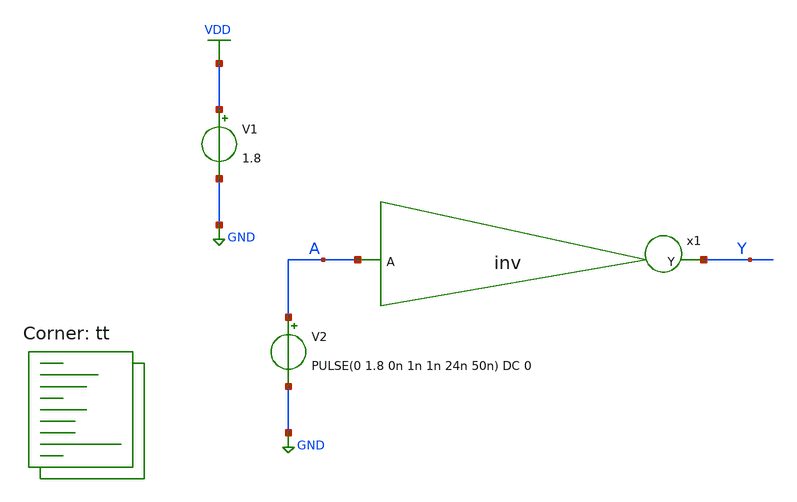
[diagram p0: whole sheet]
** sch_path: eng331lab_final/eng331lab_xschem/tb_inv2.sch
**.subckt tb_inv2
V1 VDD GND 1.8
V2 A GND PULSE(0 1.8 0n 1n 1n 24n 50n) DC 0
x1 Y A inv
**** begin user architecture code

.control
  save all
  tran 10n 400n
  write tb_inv2.raw
  set appendwirte
.endc


.lib $::SKYWATER_MODELS/sky130.lib.spice tt
**** end user architecture code
**.ends

* expanding   symbol:  eng331lab_xschem/inv.sym # of pins=2
** sym_path: eng331lab_final/eng331lab_xschem/inv.sym
** sch_path: eng331lab_final/eng331lab_xschem/inv.sch
.subckt inv Y A
*.ipin A
*.opin Y
XM1 Y A VDD VDD sky130_fd_pr__pfet_01v8 L=0.15 W=0.8 nf=1 ad='int((1 + 1)/2) * 0.8 / 1 * 0.29' as='int((1 + 2)/2) * 0.8 / 1 * 0.29'
+ pd='2*int((1 + 1)/2) * (0.8 / 1 + 0.29)' ps='2*int((1 + 2)/2) * (0.8 / 1 + 0.29)' nrd='0.29 / 0.8 ' nrs='0.29 / 0.8 '
+ sa=0 sb=0 sd=0 mult=1 m=1
XM2 Y A GND GND sky130_fd_pr__nfet_01v8 L=0.15 W=0.5 nf=1 ad='int((1 + 1)/2) * 0.5 / 1 * 0.29' as='int((1 + 2)/2) * 0.5 / 1 * 0.29'
+ pd='2*int((1 + 1)/2) * (0.5 / 1 + 0.29)' ps='2*int((1 + 2)/2) * (0.5 / 1 + 0.29)' nrd='0.29 / 0.5 ' nrs='0.29 / 0.5 '
+ sa=0 sb=0 sd=0 mult=1 m=1
.ends

.GLOBAL VDD
.GLOBAL GND
.end
